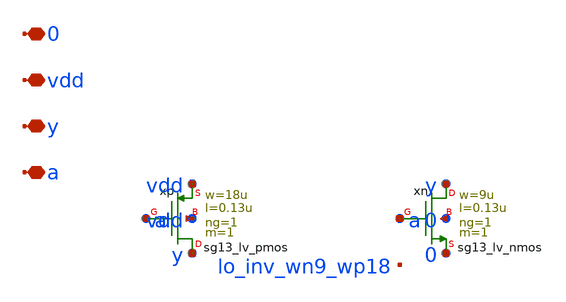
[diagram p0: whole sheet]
** sch_path: analog/lo/sch/lo_inv_9_18.sch
**.subckt lo_inv_9_18 a y vdd 0
*.iopin a
*.iopin y
*.iopin vdd
*.iopin 0
Xxp y a vdd vdd sg13_lv_pmos w=18u l=0.13u ng=1 m=1 mm_ok=1
Xxn y a 0 0 sg13_lv_nmos w=9u l=0.13u ng=1 m=1 mm_ok=1
**.ends
.end
